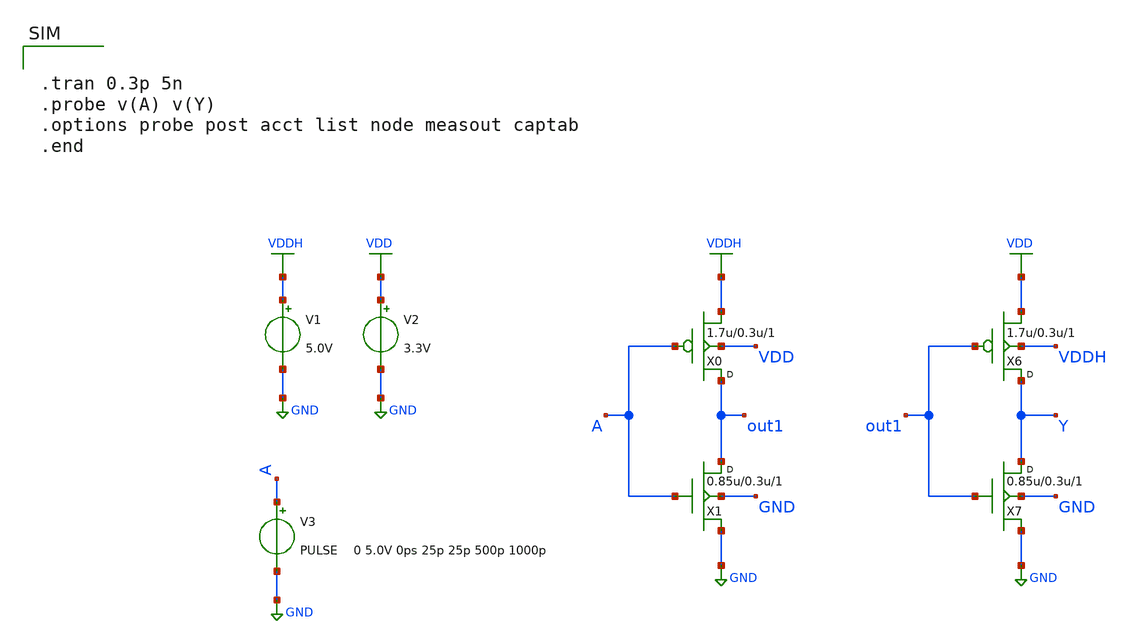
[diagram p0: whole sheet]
** sch_path: gf180mcu_osu_sc_gp12t3v3/cells/lshifdown/gf180mcu_osu_sc_gp12t3v3__lshifdown.sch
**.subckt gf180mcu_osu_sc_gp12t3v3__lshifdown
X0 out1 A VDDH VDD pfet_03p3 w=1.7u l=0.3u m=1
X1 out1 A GND GND nfet_03p3 w=0.85u l=0.3u m=1
X6 Y out1 VDD VDDH pfet_03p3 w=1.7u l=0.3u m=1
X7 Y out1 GND GND nfet_03p3 w=0.85u l=0.3u m=1
V1 VDDH GND 5.0V
V2 VDD GND 3.3V
V3 A GND PULSE 0 5.0V 0ps 25p 25p 500p 1000p
**** begin user architecture code

.temp 25
.inc "/import/yukari1/lrburle/OSU_180/char/techfiles/design.hspice"
.lib "/import/yukari1/lrburle/OSU_180/char/techfiles/sm141064.hspice" typical



.tran 0.3p 5n
.probe v(A) v(Y)
.options probe post acct list node measout captab
.end


**** end user architecture code
**.ends
.GLOBAL VDDH
.GLOBAL GND
.GLOBAL VDD
.end
